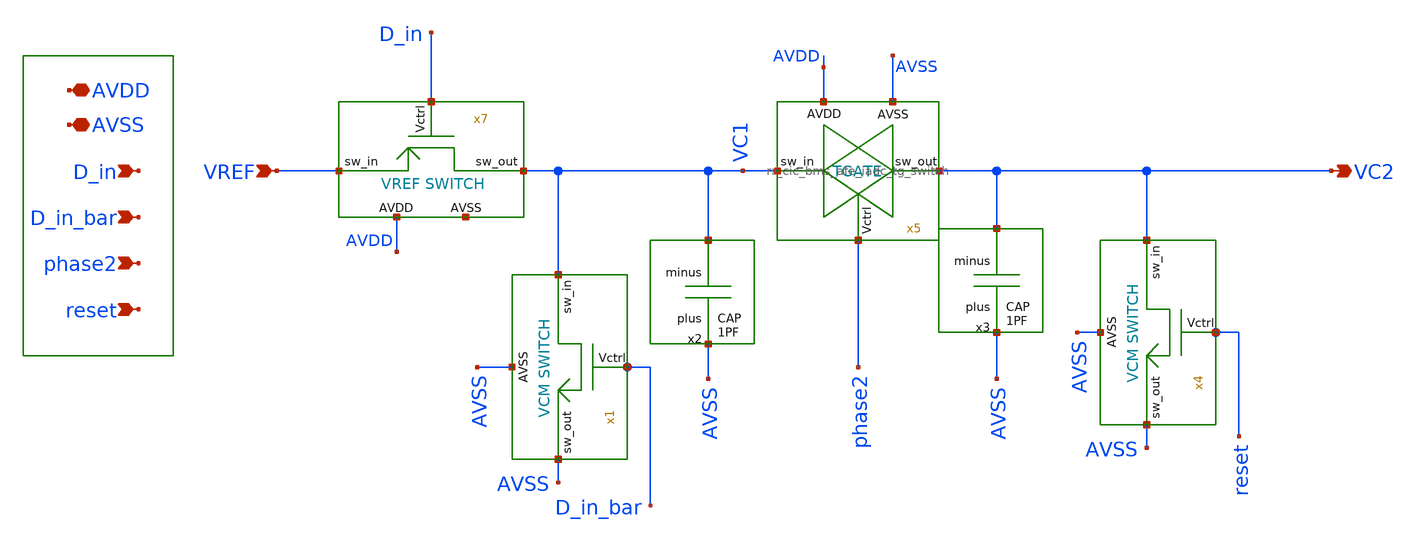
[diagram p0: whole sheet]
** sch_path: design/schematics/EIS/pkr_eis_2c_DAC.sch
**.subckt pkr_eis_2c_DAC D_in_bar AVDD VC2 phase2 D_in reset AVSS VREF
*.ipin D_in_bar
*.iopin AVDD
*.opin VC2
*.ipin phase2
*.ipin D_in
*.ipin reset
*.iopin AVSS
*.ipin VREF
x5 AVDD phase2 VC1 VC2 AVSS rr_cic_bms_afe_iadc_tg_switch
x7 net1 AVDD D_in VC1 VREF rr_cic_bms_afe_iadc_vref_switch
x2 AVSS VC1 pkr_eis_2c_DAC_cap
x3 AVSS VC2 pkr_eis_2c_DAC_cap
x1 AVSS D_in_bar AVSS VC1 rr_cic_bms_afe_iadc_vcm_switch
x4 AVSS reset AVSS VC2 rr_cic_bms_afe_iadc_vcm_switch
**.ends
.end
